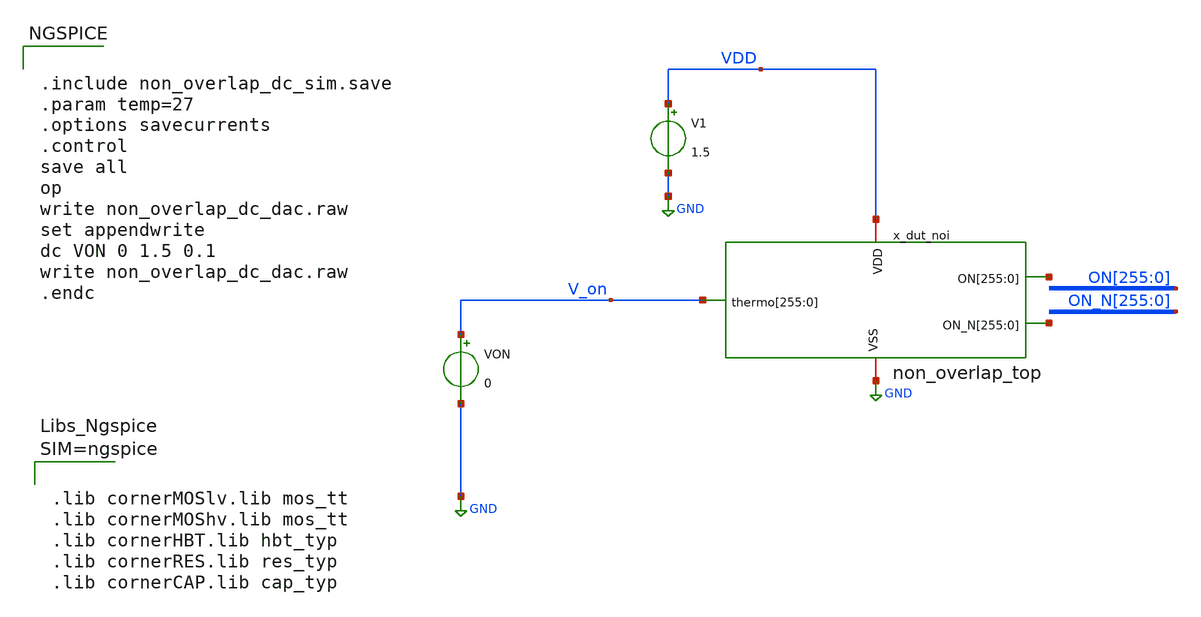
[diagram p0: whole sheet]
** sch_path: xschem/non_overlap_dc_sim.sch
**.subckt non_overlap_dc_sim
V1 VDD GND 1.5
.save i(v1)
VON V_on GND 0
.save i(von)
x_dut_noi VDD net1[255] net1[254] net1[253] net1[252] net1[251] net1[250] net1[249] net1[248]
+ net1[247] net1[246] net1[245] net1[244] net1[243] net1[242] net1[241] net1[240] net1[239] net1[238] net1[237]
+ net1[236] net1[235] net1[234] net1[233] net1[232] net1[231] net1[230] net1[229] net1[228] net1[227] net1[226]
+ net1[225] net1[224] net1[223] net1[222] net1[221] net1[220] net1[219] net1[218] net1[217] net1[216] net1[215]
+ net1[214] net1[213] net1[212] net1[211] net1[210] net1[209] net1[208] net1[207] net1[206] net1[205] net1[204]
+ net1[203] net1[202] net1[201] net1[200] net1[199] net1[198] net1[197] net1[196] net1[195] net1[194] net1[193]
+ net1[192] net1[191] net1[190] net1[189] net1[188] net1[187] net1[186] net1[185] net1[184] net1[183] net1[182]
+ net1[181] net1[180] net1[179] net1[178] net1[177] net1[176] net1[175] net1[174] net1[173] net1[172] net1[171]
+ net1[170] net1[169] net1[168] net1[167] net1[166] net1[165] net1[164] net1[163] net1[162] net1[161] net1[160]
+ net1[159] net1[158] net1[157] net1[156] net1[155] net1[154] net1[153] net1[152] net1[151] net1[150] net1[149]
+ net1[148] net1[147] net1[146] net1[145] net1[144] net1[143] net1[142] net1[141] net1[140] net1[139] net1[138]
+ net1[137] net1[136] net1[135] net1[134] net1[133] net1[132] net1[131] net1[130] net1[129] net1[128] net1[127]
+ net1[126] net1[125] net1[124] net1[123] net1[122] net1[121] net1[120] net1[119] net1[118] net1[117] net1[116]
+ net1[115] net1[114] net1[113] net1[112] net1[111] net1[110] net1[109] net1[108] net1[107] net1[106] net1[105]
+ net1[104] net1[103] net1[102] net1[101] net1[100] net1[99] net1[98] net1[97] net1[96] net1[95] net1[94]
+ net1[93] net1[92] net1[91] net1[90] net1[89] net1[88] net1[87] net1[86] net1[85] net1[84] net1[83] net1[82]
+ net1[81] net1[80] net1[79] net1[78] net1[77] net1[76] net1[75] net1[74] net1[73] net1[72] net1[71] net1[70]
+ net1[69] net1[68] net1[67] net1[66] net1[65] net1[64] net1[63] net1[62] net1[61] net1[60] net1[59] net1[58]
+ net1[57] net1[56] net1[55] net1[54] net1[53] net1[52] net1[51] net1[50] net1[49] net1[48] net1[47] net1[46]
+ net1[45] net1[44] net1[43] net1[42] net1[41] net1[40] net1[39] net1[38] net1[37] net1[36] net1[35] net1[34]
+ net1[33] net1[32] net1[31] net1[30] net1[29] net1[28] net1[27] net1[26] net1[25] net1[24] net1[23] net1[22]
+ net1[21] net1[20] net1[19] net1[18] net1[17] net1[16] net1[15] net1[14] net1[13] net1[12] net1[11] net1[10]
+ net1[9] net1[8] net1[7] net1[6] net1[5] net1[4] net1[3] net1[2] net1[1] net1[0] V_on V_on V_on V_on V_on
+ V_on V_on V_on V_on V_on V_on V_on V_on V_on V_on V_on V_on V_on V_on V_on V_on V_on V_on V_on V_on V_on
+ V_on V_on V_on V_on V_on V_on V_on V_on V_on V_on V_on V_on V_on V_on V_on V_on V_on V_on V_on V_on V_on
+ V_on V_on V_on V_on V_on V_on V_on V_on V_on V_on V_on V_on V_on V_on V_on V_on V_on V_on V_on V_on V_on
+ V_on V_on V_on V_on V_on V_on V_on V_on V_on V_on V_on V_on V_on V_on V_on V_on V_on V_on V_on V_on V_on
+ V_on V_on V_on V_on V_on V_on V_on V_on V_on V_on V_on V_on V_on V_on V_on V_on V_on V_on V_on V_on V_on
+ V_on V_on V_on V_on V_on V_on V_on V_on V_on V_on V_on V_on V_on V_on V_on V_on V_on V_on V_on V_on V_on
+ V_on V_on V_on V_on V_on V_on V_on V_on V_on V_on V_on V_on V_on V_on V_on V_on V_on V_on V_on V_on V_on
+ V_on V_on V_on V_on V_on V_on V_on V_on V_on V_on V_on V_on V_on V_on V_on V_on V_on V_on V_on V_on V_on
+ V_on V_on V_on V_on V_on V_on V_on V_on V_on V_on V_on V_on V_on V_on V_on V_on V_on V_on V_on V_on V_on
+ V_on V_on V_on V_on V_on V_on V_on V_on V_on V_on V_on V_on V_on V_on V_on V_on V_on V_on V_on V_on V_on
+ V_on V_on V_on V_on V_on V_on V_on V_on V_on V_on V_on V_on V_on V_on V_on V_on V_on V_on V_on V_on V_on
+ V_on V_on V_on V_on V_on V_on V_on V_on V_on V_on V_on V_on V_on V_on V_on V_on V_on V_on V_on V_on
+ net2[255] net2[254] net2[253] net2[252] net2[251] net2[250] net2[249] net2[248] net2[247] net2[246] net2[245]
+ net2[244] net2[243] net2[242] net2[241] net2[240] net2[239] net2[238] net2[237] net2[236] net2[235] net2[234]
+ net2[233] net2[232] net2[231] net2[230] net2[229] net2[228] net2[227] net2[226] net2[225] net2[224] net2[223]
+ net2[222] net2[221] net2[220] net2[219] net2[218] net2[217] net2[216] net2[215] net2[214] net2[213] net2[212]
+ net2[211] net2[210] net2[209] net2[208] net2[207] net2[206] net2[205] net2[204] net2[203] net2[202] net2[201]
+ net2[200] net2[199] net2[198] net2[197] net2[196] net2[195] net2[194] net2[193] net2[192] net2[191] net2[190]
+ net2[189] net2[188] net2[187] net2[186] net2[185] net2[184] net2[183] net2[182] net2[181] net2[180] net2[179]
+ net2[178] net2[177] net2[176] net2[175] net2[174] net2[173] net2[172] net2[171] net2[170] net2[169] net2[168]
+ net2[167] net2[166] net2[165] net2[164] net2[163] net2[162] net2[161] net2[160] net2[159] net2[158] net2[157]
+ net2[156] net2[155] net2[154] net2[153] net2[152] net2[151] net2[150] net2[149] net2[148] net2[147] net2[146]
+ net2[145] net2[144] net2[143] net2[142] net2[141] net2[140] net2[139] net2[138] net2[137] net2[136] net2[135]
+ net2[134] net2[133] net2[132] net2[131] net2[130] net2[129] net2[128] net2[127] net2[126] net2[125] net2[124]
+ net2[123] net2[122] net2[121] net2[120] net2[119] net2[118] net2[117] net2[116] net2[115] net2[114] net2[113]
+ net2[112] net2[111] net2[110] net2[109] net2[108] net2[107] net2[106] net2[105] net2[104] net2[103] net2[102]
+ net2[101] net2[100] net2[99] net2[98] net2[97] net2[96] net2[95] net2[94] net2[93] net2[92] net2[91] net2[90]
+ net2[89] net2[88] net2[87] net2[86] net2[85] net2[84] net2[83] net2[82] net2[81] net2[80] net2[79] net2[78]
+ net2[77] net2[76] net2[75] net2[74] net2[73] net2[72] net2[71] net2[70] net2[69] net2[68] net2[67] net2[66]
+ net2[65] net2[64] net2[63] net2[62] net2[61] net2[60] net2[59] net2[58] net2[57] net2[56] net2[55] net2[54]
+ net2[53] net2[52] net2[51] net2[50] net2[49] net2[48] net2[47] net2[46] net2[45] net2[44] net2[43] net2[42]
+ net2[41] net2[40] net2[39] net2[38] net2[37] net2[36] net2[35] net2[34] net2[33] net2[32] net2[31] net2[30]
+ net2[29] net2[28] net2[27] net2[26] net2[25] net2[24] net2[23] net2[22] net2[21] net2[20] net2[19] net2[18]
+ net2[17] net2[16] net2[15] net2[14] net2[13] net2[12] net2[11] net2[10] net2[9] net2[8] net2[7] net2[6]
+ net2[5] net2[4] net2[3] net2[2] net2[1] net2[0] GND non_overlap_top
**** begin user architecture code


.include non_overlap_dc_sim.save
.param temp=27
.options savecurrents
.control
save all
op
write non_overlap_dc_dac.raw
set appendwrite
dc VON 0 1.5 0.1
write non_overlap_dc_dac.raw
.endc





.lib cornerMOSlv.lib mos_tt
.lib cornerMOShv.lib mos_tt
.lib cornerHBT.lib hbt_typ
.lib cornerRES.lib res_typ
.lib cornerCAP.lib cap_typ



**** end user architecture code
**.ends
.GLOBAL GND
.end
